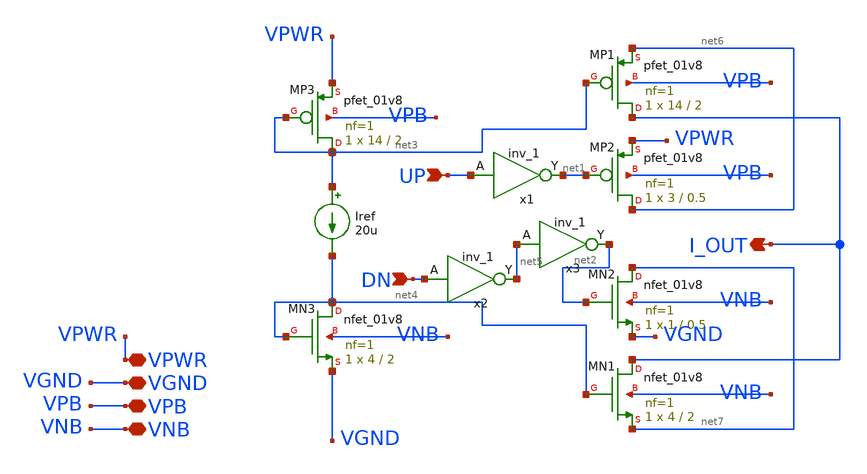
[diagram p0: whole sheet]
** sch_path: cp.sch
**.subckt cp UP DN VPWR VGND VPB VNB I_OUT
*.ipin UP
*.ipin DN
*.iopin VPWR
*.iopin VGND
*.iopin VPB
*.iopin VNB
*.opin I_OUT
XMN1 I_OUT net4 net7 VNB sky130_fd_pr__nfet_01v8 L=2 W=4 nf=1 ad='int((1 + 1)/2) * 4 / 1 * 0.29' as='int((1 + 2)/2) * 4 / 1 * 0.29'
+ pd='2*int((1 + 1)/2) * (4 / 1 + 0.29)' ps='2*int((1 + 2)/2) * (4 / 1 + 0.29)' nrd='0.29 / 4 ' nrs='0.29 / 4 '
+ sa=0 sb=0 sd=0 mult=1 m=1
XMP1 I_OUT net3 net6 VPB sky130_fd_pr__pfet_01v8 L=2 W=14 nf=1 ad='int((1 + 1)/2) * 14 / 1 * 0.29' as='int((1 + 2)/2) * 14 / 1 * 0.29'
+ pd='2*int((1 + 1)/2) * (14 / 1 + 0.29)' ps='2*int((1 + 2)/2) * (14 / 1 + 0.29)' nrd='0.29 / 14 ' nrs='0.29 / 14 '
+ sa=0 sb=0 sd=0 mult=1 m=1
Iref net3 net4 20u
XMN2 net7 net2 VGND VNB sky130_fd_pr__nfet_01v8 L=0.5 W=1 nf=1 ad='int((1 + 1)/2) * 1 / 1 * 0.29' as='int((1 + 2)/2) * 1 / 1 * 0.29'
+ pd='2*int((1 + 1)/2) * (1 / 1 + 0.29)' ps='2*int((1 + 2)/2) * (1 / 1 + 0.29)' nrd='0.29 / 1 ' nrs='0.29 / 1 '
+ sa=0 sb=0 sd=0 mult=1 m=1
XMP2 net6 net1 VPWR VPB sky130_fd_pr__pfet_01v8 L=0.5 W=3 nf=1 ad='int((1 + 1)/2) * 3 / 1 * 0.29' as='int((1 + 2)/2) * 3 / 1 * 0.29'
+ pd='2*int((1 + 1)/2) * (3 / 1 + 0.29)' ps='2*int((1 + 2)/2) * (3 / 1 + 0.29)' nrd='0.29 / 3 ' nrs='0.29 / 3 '
+ sa=0 sb=0 sd=0 mult=1 m=1
x1 UP VGND VNB VPB VPWR net1 sky130_fd_sc_hd__inv_1
XMP3 net3 net3 VPWR VPB sky130_fd_pr__pfet_01v8 L=2 W=14 nf=1 ad='int((1 + 1)/2) * 14 / 1 * 0.29' as='int((1 + 2)/2) * 14 / 1 * 0.29'
+ pd='2*int((1 + 1)/2) * (14 / 1 + 0.29)' ps='2*int((1 + 2)/2) * (14 / 1 + 0.29)' nrd='0.29 / 14 ' nrs='0.29 / 14 '
+ sa=0 sb=0 sd=0 mult=1 m=1
XMN3 net4 net4 VGND VNB sky130_fd_pr__nfet_01v8 L=2 W=4 nf=1 ad='int((1 + 1)/2) * 4 / 1 * 0.29' as='int((1 + 2)/2) * 4 / 1 * 0.29'
+ pd='2*int((1 + 1)/2) * (4 / 1 + 0.29)' ps='2*int((1 + 2)/2) * (4 / 1 + 0.29)' nrd='0.29 / 4 ' nrs='0.29 / 4 '
+ sa=0 sb=0 sd=0 mult=1 m=1
x2 DN VGND VNB VPB VPWR net5 sky130_fd_sc_hd__inv_1
x3 net5 VGND VNB VPB VPWR net2 sky130_fd_sc_hd__inv_1
**.ends
.end
